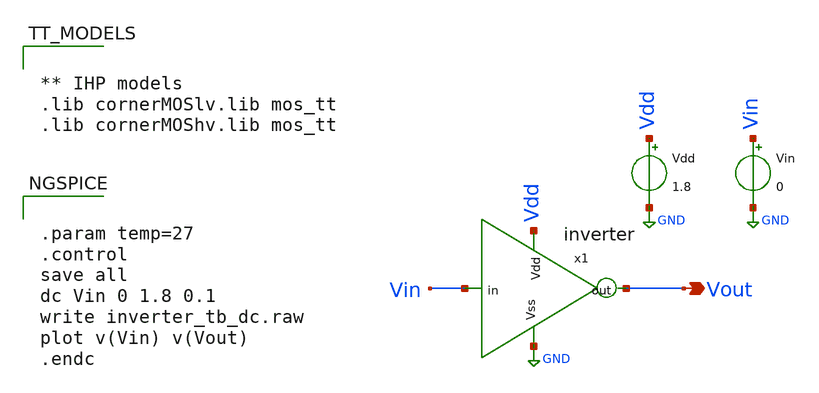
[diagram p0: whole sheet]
** sch_path: inverter/xschem/inverter_tb_dc.sch
**.subckt inverter_tb_dc Vout
*.opin Vout
x1 Vdd Vin Vout GND inverter
Vdd Vdd GND 1.8
Vin Vin GND 0
**** begin user architecture code


** IHP models
.lib cornerMOSlv.lib mos_tt
.lib cornerMOShv.lib mos_tt




.param temp=27
.control
save all
dc Vin 0 1.8 0.1
write inverter_tb_dc.raw
plot v(Vin) v(Vout)
.endc


**** end user architecture code
**.ends

* expanding   symbol:  practicing/inverter/xschem/inverter.sym # of pins=4
** sym_path: inverter/xschem/inverter.sym
** sch_path: inverter/xschem/inverter.sch
.subckt inverter vdd in out vss
*.iopin vdd
*.iopin vss
*.ipin in
*.opin out
XM1 out in vss vss sg13_lv_nmos w=0.15u l=0.13u ng=1 m=1 mm_ok=1
XM2 out in vdd vdd sg13_lv_pmos w=0.15u l=0.13u ng=1 m=1 mm_ok=1
.ends

.GLOBAL GND
.end
